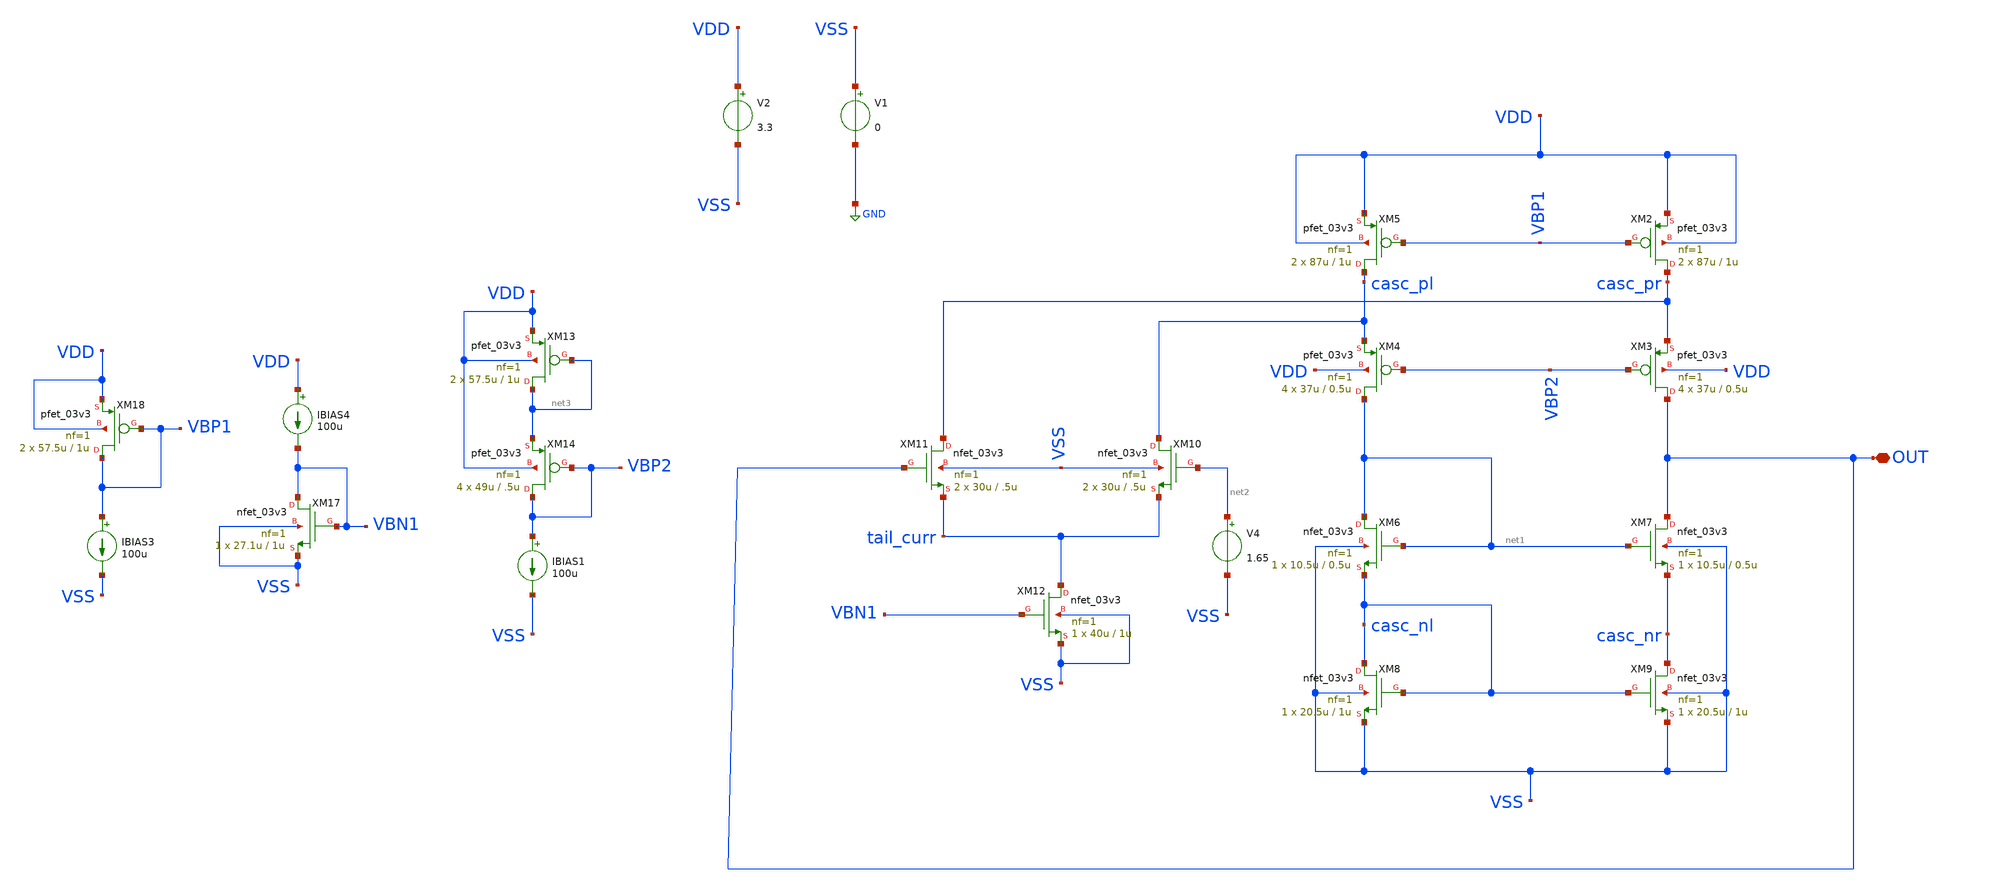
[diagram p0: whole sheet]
** sch_path: designs/libs/core_amps/ota_folded_cascode/etj_folded_new_vdsat.sch
**.subckt etj_folded_new_vdsat OUT
*.iopin OUT
XM2 casc_pr VBP1 VDD VDD pfet_03v3 L=1u W=87u nf=1 ad='int((nf+1)/2) * W/nf * 0.18u' as='int((nf+2)/2) * W/nf * 0.18u'
+ pd='2*int((nf+1)/2) * (W/nf + 0.18u)' ps='2*int((nf+2)/2) * (W/nf + 0.18u)' nrd='0.18u / W' nrs='0.18u / W'
+ sa=0 sb=0 sd=0 m=2
XM3 OUT VBP2 casc_pr VDD pfet_03v3 L=0.5u W=37u nf=1 ad='int((nf+1)/2) * W/nf * 0.18u' as='int((nf+2)/2) * W/nf * 0.18u'
+ pd='2*int((nf+1)/2) * (W/nf + 0.18u)' ps='2*int((nf+2)/2) * (W/nf + 0.18u)' nrd='0.18u / W' nrs='0.18u / W'
+ sa=0 sb=0 sd=0 m=4
XM4 net1 VBP2 casc_pl VDD pfet_03v3 L=0.5u W=37u nf=1 ad='int((nf+1)/2) * W/nf * 0.18u' as='int((nf+2)/2) * W/nf * 0.18u'
+ pd='2*int((nf+1)/2) * (W/nf + 0.18u)' ps='2*int((nf+2)/2) * (W/nf + 0.18u)' nrd='0.18u / W' nrs='0.18u / W'
+ sa=0 sb=0 sd=0 m=4
XM5 casc_pl VBP1 VDD VDD pfet_03v3 L=1u W=87u nf=1 ad='int((nf+1)/2) * W/nf * 0.18u' as='int((nf+2)/2) * W/nf * 0.18u'
+ pd='2*int((nf+1)/2) * (W/nf + 0.18u)' ps='2*int((nf+2)/2) * (W/nf + 0.18u)' nrd='0.18u / W' nrs='0.18u / W'
+ sa=0 sb=0 sd=0 m=2
XM6 net1 net1 casc_nl VSS nfet_03v3 L=0.5u W=10.5u nf=1 ad='int((nf+1)/2) * W/nf * 0.18u' as='int((nf+2)/2) * W/nf * 0.18u'
+ pd='2*int((nf+1)/2) * (W/nf + 0.18u)' ps='2*int((nf+2)/2) * (W/nf + 0.18u)' nrd='0.18u / W' nrs='0.18u / W'
+ sa=0 sb=0 sd=0 m=1
XM7 OUT net1 casc_nr VSS nfet_03v3 L=0.5u W=10.5u nf=1 ad='int((nf+1)/2) * W/nf * 0.18u' as='int((nf+2)/2) * W/nf * 0.18u'
+ pd='2*int((nf+1)/2) * (W/nf + 0.18u)' ps='2*int((nf+2)/2) * (W/nf + 0.18u)' nrd='0.18u / W' nrs='0.18u / W'
+ sa=0 sb=0 sd=0 m=1
XM8 casc_nl casc_nl VSS VSS nfet_03v3 L=1u W=20.5u nf=1 ad='int((nf+1)/2) * W/nf * 0.18u' as='int((nf+2)/2) * W/nf * 0.18u'
+ pd='2*int((nf+1)/2) * (W/nf + 0.18u)' ps='2*int((nf+2)/2) * (W/nf + 0.18u)' nrd='0.18u / W' nrs='0.18u / W'
+ sa=0 sb=0 sd=0 m=1
XM9 casc_nr casc_nl VSS VSS nfet_03v3 L=1u W=20.5u nf=1 ad='int((nf+1)/2) * W/nf * 0.18u' as='int((nf+2)/2) * W/nf * 0.18u'
+ pd='2*int((nf+1)/2) * (W/nf + 0.18u)' ps='2*int((nf+2)/2) * (W/nf + 0.18u)' nrd='0.18u / W' nrs='0.18u / W'
+ sa=0 sb=0 sd=0 m=1
XM10 casc_pl net2 tail_curr VSS nfet_03v3 L=.5u W=30u nf=1 ad='int((nf+1)/2) * W/nf * 0.18u' as='int((nf+2)/2) * W/nf * 0.18u'
+ pd='2*int((nf+1)/2) * (W/nf + 0.18u)' ps='2*int((nf+2)/2) * (W/nf + 0.18u)' nrd='0.18u / W' nrs='0.18u / W'
+ sa=0 sb=0 sd=0 m=2
XM12 tail_curr VBN1 VSS VSS nfet_03v3 L=1u W=40u nf=1 ad='int((nf+1)/2) * W/nf * 0.18u' as='int((nf+2)/2) * W/nf * 0.18u'
+ pd='2*int((nf+1)/2) * (W/nf + 0.18u)' ps='2*int((nf+2)/2) * (W/nf + 0.18u)' nrd='0.18u / W' nrs='0.18u / W'
+ sa=0 sb=0 sd=0 m=1
XM11 casc_pr OUT tail_curr VSS nfet_03v3 L=.5u W=30u nf=1 ad='int((nf+1)/2) * W/nf * 0.18u' as='int((nf+2)/2) * W/nf * 0.18u'
+ pd='2*int((nf+1)/2) * (W/nf + 0.18u)' ps='2*int((nf+2)/2) * (W/nf + 0.18u)' nrd='0.18u / W' nrs='0.18u / W'
+ sa=0 sb=0 sd=0 m=2
V2 VDD VSS 3.3
V1 VSS GND 0
V4 net2 VSS 1.65
XM13 net3 net3 VDD VDD pfet_03v3 L=1u W=57.5u nf=1 ad='int((nf+1)/2) * W/nf * 0.18u' as='int((nf+2)/2) * W/nf * 0.18u'
+ pd='2*int((nf+1)/2) * (W/nf + 0.18u)' ps='2*int((nf+2)/2) * (W/nf + 0.18u)' nrd='0.18u / W' nrs='0.18u / W'
+ sa=0 sb=0 sd=0 m=2
IBIAS1 VBP2 VSS 100u
XM14 VBP2 VBP2 net3 VDD pfet_03v3 L=.5u W=49u nf=1 ad='int((nf+1)/2) * W/nf * 0.18u' as='int((nf+2)/2) * W/nf * 0.18u'
+ pd='2*int((nf+1)/2) * (W/nf + 0.18u)' ps='2*int((nf+2)/2) * (W/nf + 0.18u)' nrd='0.18u / W' nrs='0.18u / W'
+ sa=0 sb=0 sd=0 m=4
XM17 VBN1 VBN1 VSS VSS nfet_03v3 L=1u W=27.1u nf=1 ad='int((nf+1)/2) * W/nf * 0.18u' as='int((nf+2)/2) * W/nf * 0.18u'
+ pd='2*int((nf+1)/2) * (W/nf + 0.18u)' ps='2*int((nf+2)/2) * (W/nf + 0.18u)' nrd='0.18u / W' nrs='0.18u / W'
+ sa=0 sb=0 sd=0 m=1
XM18 VBP1 VBP1 VDD VDD pfet_03v3 L=1u W=57.5u nf=1 ad='int((nf+1)/2) * W/nf * 0.18u' as='int((nf+2)/2) * W/nf * 0.18u'
+ pd='2*int((nf+1)/2) * (W/nf + 0.18u)' ps='2*int((nf+2)/2) * (W/nf + 0.18u)' nrd='0.18u / W' nrs='0.18u / W'
+ sa=0 sb=0 sd=0 m=2
IBIAS3 VBP1 VSS 100u
IBIAS4 VDD VBN1 100u
**** begin user architecture code

.include $::180MCU_MODELS/design.ngspice
.lib $::180MCU_MODELS/sm141064.ngspice typical



.control

op

let sat_xm17 = abs(@m.xm17.m0[vds]) - abs(@m.xm17.m0[vdsat])
let sat_xm16 = abs(@m.xm16.m0[vds]) - abs(@m.xm16.m0[vdsat])
let sat_xm15 = abs(@m.xm15.m0[vds]) - abs(@m.xm15.m0[vdsat])
let sat_xm11 = abs(@m.xm11.m0[vds]) - abs(@m.xm11.m0[vdsat])
let sat_xm12 = abs(@m.xm12.m0[vds]) - abs(@m.xm12.m0[vdsat])
let sat_xm10 = abs(@m.xm10.m0[vds]) - abs(@m.xm10.m0[vdsat])
let sat_xm9  = abs(@m.xm9.m0[vds]) - abs(@m.xm9.m0[vdsat])
let sat_xm8  = abs(@m.xm8.m0[vds]) - abs(@m.xm8.m0[vdsat])
let sat_xm7  = abs(@m.xm7.m0[vds]) - abs(@m.xm7.m0[vdsat])
let sat_xm6  = abs(@m.xm6.m0[vds]) - abs(@m.xm6.m0[vdsat])
let sat_xm18 = abs(@m.xm18.m0[vds]) - abs(@m.xm18.m0[vdsat])
let sat_xm14 = abs(@m.xm14.m0[vds]) - abs(@m.xm14.m0[vdsat])
let sat_xm13 = abs(@m.xm13.m0[vds]) - abs(@m.xm13.m0[vdsat])
let sat_xm5  = abs(@m.xm5.m0[vds]) - abs(@m.xm5.m0[vdsat])
let sat_xm4  = abs(@m.xm4.m0[vds]) - abs(@m.xm4.m0[vdsat])
let sat_xm3  = abs(@m.xm3.m0[vds]) - abs(@m.xm3.m0[vdsat])
let sat_xm2  = abs(@m.xm2.m0[vds]) - abs(@m.xm2.m0[vdsat])
print sat_xm17 sat_xm16 sat_xm15 sat_xm11 sat_xm12
print sat_xm10 sat_xm9 sat_xm8 sat_xm7 sat_xm6
print sat_xm18 sat_xm14 sat_xm13 sat_xm5 sat_xm4
print sat_xm3 sat_xm2

.endc


**** end user architecture code
**.ends
.GLOBAL GND
.end
